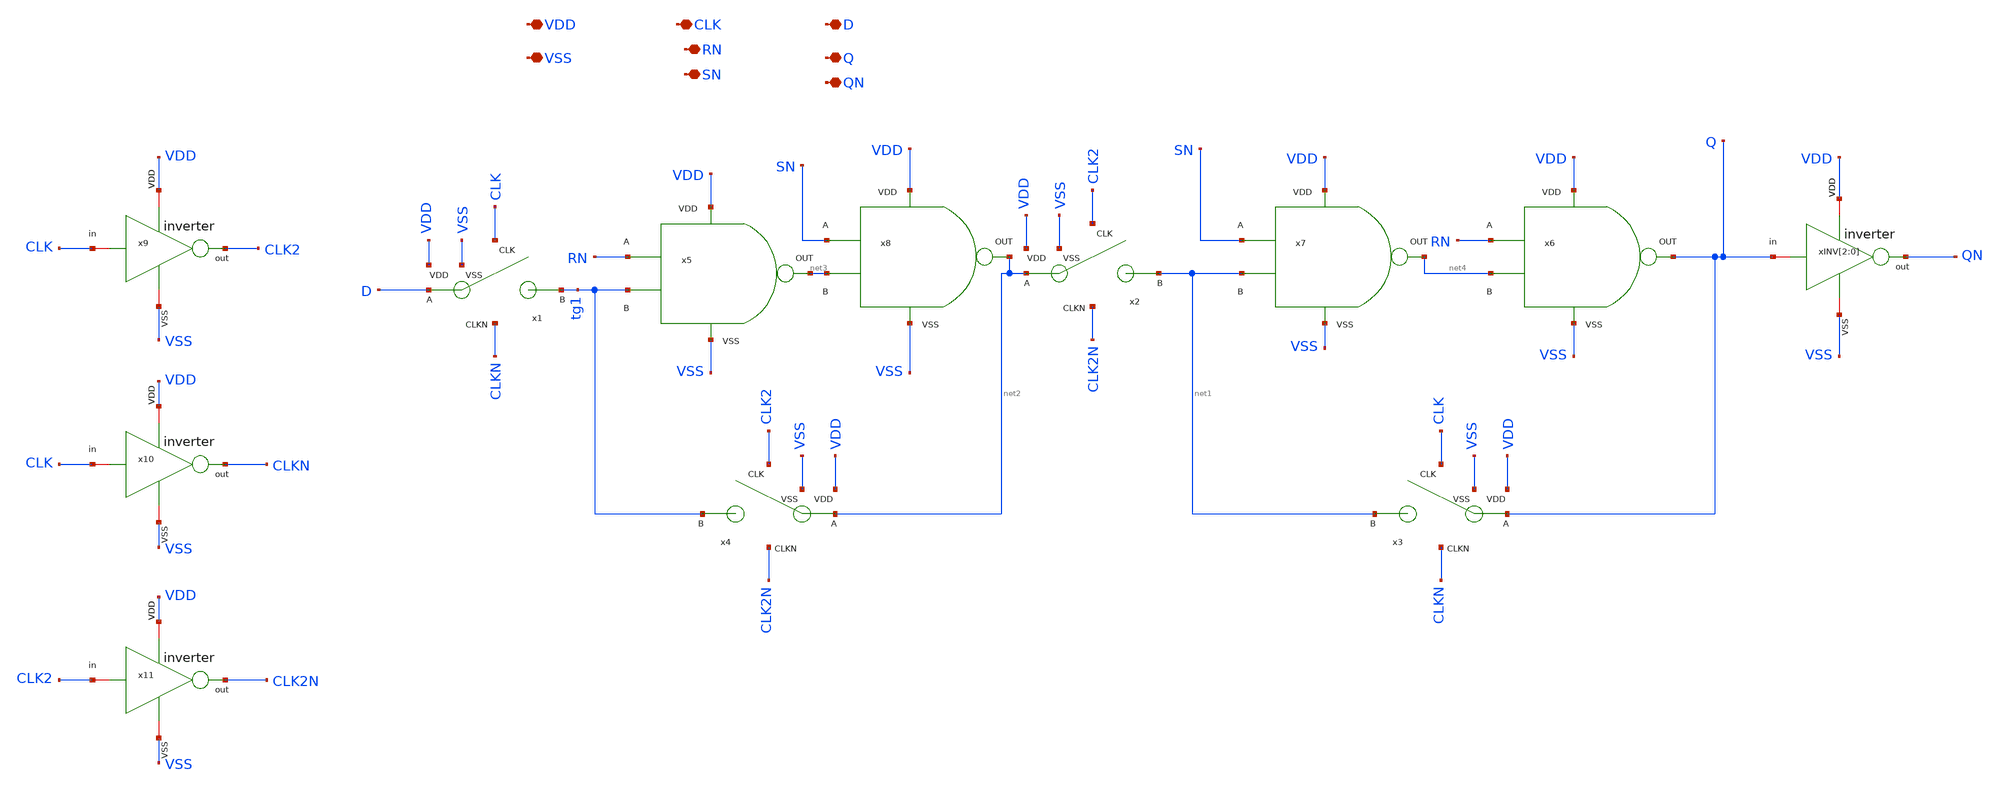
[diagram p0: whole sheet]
** sch_path: designs/sar_adc/digital/flip_flop_set/xschem/flip_flop_set.sch
**.subckt flip_flop_set VDD VSS CLK D RN Q QN SN
*.iopin VDD
*.iopin VSS
*.iopin CLK
*.iopin D
*.iopin RN
*.iopin Q
*.iopin QN
*.iopin SN
x1 CLK D VDD tg1 CLKN VSS TG
x2 CLK2 net2 VDD net1 CLK2N VSS TG
x3 CLK Q VDD net1 CLKN VSS TG
x4 CLK2 net2 VDD tg1 CLK2N VSS TG
x5 VDD VSS RN tg1 net3 NAND
x6 VDD VSS RN net4 Q NAND
x9 VDD CLK CLK2 VSS inverter
x10 VDD CLK CLKN VSS inverter
x11 VDD CLK2 CLK2N VSS inverter
xINV[2] VDD Q QN VSS inverter
xINV[1] VDD Q QN VSS inverter
xINV[0] VDD Q QN VSS inverter
x8 VDD VSS SN net3 net2 NAND
x7 VDD VSS SN net1 net4 NAND
**.ends

* expanding   symbol:  designs/sar_adc/digital/TG/xschem/TG.sym # of pins=6
** sym_path: designs/sar_adc/digital/TG/xschem/TG.sym
** sch_path: designs/sar_adc/digital/TG/xschem/TG.sch
.subckt TG CLK A VDD B CLKN VSS
*.iopin VDD
*.iopin VSS
*.ipin CLK
*.ipin CLKN
*.iopin A
*.iopin B
XM1 A CLK B VSS nfet_03v3 L=0.28u W=0.22u nf=1 ad='int((nf+1)/2) * W/nf * 0.18u' as='int((nf+2)/2) * W/nf * 0.18u'
+ pd='2*int((nf+1)/2) * (W/nf + 0.18u)' ps='2*int((nf+2)/2) * (W/nf + 0.18u)' nrd='0.18u / W' nrs='0.18u / W'
+ sa=0 sb=0 sd=0 m=1
XM2 A CLKN B VDD pfet_03v3 L=0.28u W=0.22u nf=1 ad='int((nf+1)/2) * W/nf * 0.18u' as='int((nf+2)/2) * W/nf * 0.18u'
+ pd='2*int((nf+1)/2) * (W/nf + 0.18u)' ps='2*int((nf+2)/2) * (W/nf + 0.18u)' nrd='0.18u / W' nrs='0.18u / W'
+ sa=0 sb=0 sd=0 m=1
.ends


* expanding   symbol:  designs/sar_adc/digital/NAND/xschem/NAND.sym # of pins=5
** sym_path: designs/sar_adc/digital/NAND/xschem/NAND.sym
** sch_path: designs/sar_adc/digital/NAND/xschem/NAND.sch
.subckt NAND VDD VSS A B out
*.iopin VDD
*.iopin A
*.iopin B
*.iopin out
*.iopin VSS
xINVA VDD net1 net2 VSS inverter
xINVB[2] VDD net2 out VSS inverter
xINVB[1] VDD net2 out VSS inverter
xINVB[0] VDD net2 out VSS inverter
XM2 net1 A VDD VDD pfet_03v3 L=0.28u W=0.5u nf=1 ad='int((nf+1)/2) * W/nf * 0.18u' as='int((nf+2)/2) * W/nf * 0.18u'
+ pd='2*int((nf+1)/2) * (W/nf + 0.18u)' ps='2*int((nf+2)/2) * (W/nf + 0.18u)' nrd='0.18u / W' nrs='0.18u / W'
+ sa=0 sb=0 sd=0 m=2
XM1 net1 A net3 VSS nfet_03v3 L=0.28u W=0.5u nf=1 ad='int((nf+1)/2) * W/nf * 0.18u' as='int((nf+2)/2) * W/nf * 0.18u'
+ pd='2*int((nf+1)/2) * (W/nf + 0.18u)' ps='2*int((nf+2)/2) * (W/nf + 0.18u)' nrd='0.18u / W' nrs='0.18u / W'
+ sa=0 sb=0 sd=0 m=1
XM3 net1 B VDD VDD pfet_03v3 L=0.28u W=0.5u nf=1 ad='int((nf+1)/2) * W/nf * 0.18u' as='int((nf+2)/2) * W/nf * 0.18u'
+ pd='2*int((nf+1)/2) * (W/nf + 0.18u)' ps='2*int((nf+2)/2) * (W/nf + 0.18u)' nrd='0.18u / W' nrs='0.18u / W'
+ sa=0 sb=0 sd=0 m=2
XM4 net3 B VSS VSS nfet_03v3 L=0.28u W=0.5u nf=1 ad='int((nf+1)/2) * W/nf * 0.18u' as='int((nf+2)/2) * W/nf * 0.18u'
+ pd='2*int((nf+1)/2) * (W/nf + 0.18u)' ps='2*int((nf+2)/2) * (W/nf + 0.18u)' nrd='0.18u / W' nrs='0.18u / W'
+ sa=0 sb=0 sd=0 m=1
.ends


* expanding   symbol:  designs/sar_adc/digital/inverter/xschem/inverter.sym # of pins=6
** sym_path: designs/sar_adc/digital/inverter/xschem/inverter.sym
** sch_path: designs/sar_adc/digital/inverter/xschem/inverter.sch
.subckt inverter VDD in out VSS
*.opin out
*.iopin in
*.iopin VDD
*.iopin VSS
XM1 out in VSS VSS nfet_03v3 L=0.28u W=1u nf=1 ad='int((nf+1)/2) * W/nf * 0.18u' as='int((nf+2)/2) * W/nf * 0.18u'
+ pd='2*int((nf+1)/2) * (W/nf + 0.18u)' ps='2*int((nf+2)/2) * (W/nf + 0.18u)' nrd='0.18u / W' nrs='0.18u / W'
+ sa=0 sb=0 sd=0 m=1
XM2 out in VDD VDD pfet_03v3 L=0.28u W=3u nf=1 ad='int((nf+1)/2) * W/nf * 0.18u' as='int((nf+2)/2) * W/nf * 0.18u'
+ pd='2*int((nf+1)/2) * (W/nf + 0.18u)' ps='2*int((nf+2)/2) * (W/nf + 0.18u)' nrd='0.18u / W' nrs='0.18u / W'
+ sa=0 sb=0 sd=0 m=1
.ends

.end
